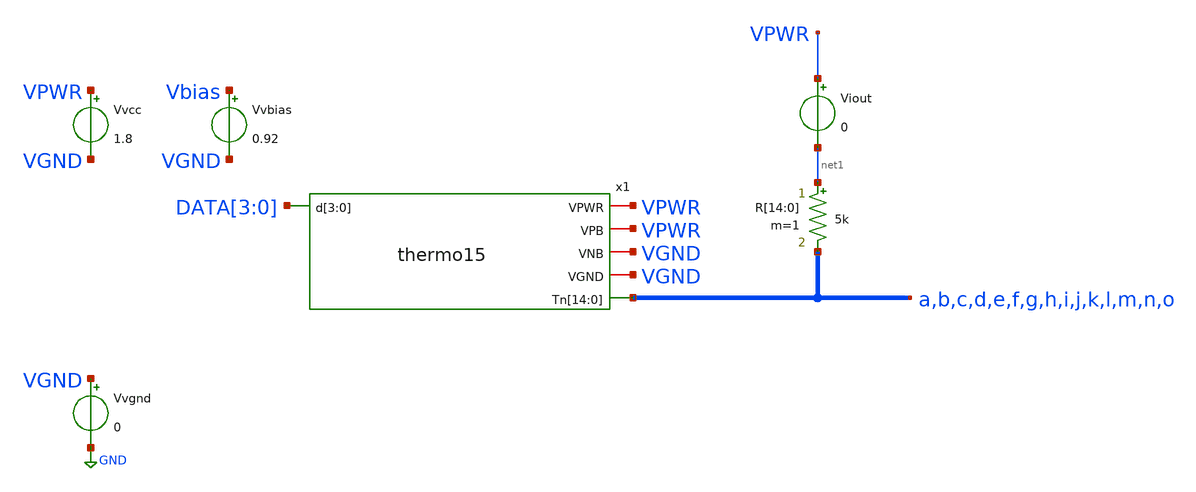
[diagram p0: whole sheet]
** sch_path: xschem/tb_thermo15.sch
**.subckt tb_thermo15
Vvcc VPWR VGND 1.8
R[14] net1 a 5k m=1
R[13] net1 b 5k m=1
R[12] net1 c 5k m=1
R[11] net1 d 5k m=1
R[10] net1 e 5k m=1
R[9] net1 f 5k m=1
R[8] net1 g 5k m=1
R[7] net1 h 5k m=1
R[6] net1 i 5k m=1
R[5] net1 j 5k m=1
R[4] net1 k 5k m=1
R[3] net1 l 5k m=1
R[2] net1 m 5k m=1
R[1] net1 n 5k m=1
R[0] net1 o 5k m=1
Vvbias Vbias VGND 0.92
Vvgnd VGND GND 0
Viout VPWR net1 0
x1 VPWR VGND VPWR VGND a b c d e f g h i j k l m n o DATA[3] DATA[2] DATA[1] DATA[0] thermo15
**** begin user architecture code



Vxp0 DATA[0]  GND pulse 1.8v 0v 0n 1n 1n 39n 80n
Vxp1 DATA[1]  GND pulse 1.8v 0v 0n 1n 1n 79n 160n
Vxp2 DATA[2]  GND pulse 1.8v 0v 0n 1n 1n 159n 320n
Vxp3 DATA[3]  GND pulse 1.8v 0v 0n 1n 1n 319n 640n

*.options savecurrents
.control

    save all
    tran 1n 12.8u
    write tb_row15x.raw a b c d e f g h i j k l m n o

.endc




.lib $::SKYWATER_MODELS/sky130.lib.spice tt
.include $::SKYWATER_STDCELLS/sky130_fd_sc_hd.spice

**** end user architecture code
**.ends

* expanding   symbol:  thermo15.sym # of pins=6
** sym_path: xschem/thermo15.sym
** sch_path: xschem/thermo15.sch
.subckt thermo15 VPWR VGND VPB VNB Tn[14] Tn[13] Tn[12] Tn[11] Tn[10] Tn[9] Tn[8] Tn[7] Tn[6] Tn[5]
+ Tn[4] Tn[3] Tn[2] Tn[1] Tn[0] d[3] d[2] d[1] d[0]
*.iopin VPWR
*.ipin d[3],d[2],d[1],d[0]
*.iopin VGND
*.iopin VPB
*.iopin VNB
*.opin
*+ Tn[14],Tn[13],Tn[12],Tn[11],Tn[10],Tn[9],Tn[8],Tn[7],Tn[6],Tn[5],Tn[4],Tn[3],Tn[2],Tn[1],Tn[0]
x1 d[1] VGND VNB VPB VPWR net3 sky130_fd_sc_hd__inv_1
x2 net5 VGND VNB VPB VPWR net6 sky130_fd_sc_hd__inv_2
x3 d[0] d[1] VGND VNB VPB VPWR net4 sky130_fd_sc_hd__nand2_1
x4 d[0] d[1] VGND VNB VPB VPWR net2 sky130_fd_sc_hd__nor2_1
x5 d[2] VGND VNB VPB VPWR net1 sky130_fd_sc_hd__inv_1
x6 net2 net1 VGND VNB VPB VPWR net7 sky130_fd_sc_hd__nand2_1
x7 net3 net1 VGND VNB VPB VPWR net8 sky130_fd_sc_hd__nand2_1
x8 net4 net1 VGND VNB VPB VPWR net9 sky130_fd_sc_hd__nand2_1
x9 net1 VGND VNB VPB VPWR net10 sky130_fd_sc_hd__inv_1
x10 net2 net1 VGND VNB VPB VPWR net11 sky130_fd_sc_hd__nor2_1
x11 net3 net1 VGND VNB VPB VPWR net12 sky130_fd_sc_hd__nor2_1
x12 net4 net1 VGND VNB VPB VPWR net13 sky130_fd_sc_hd__nor2_1
x13 net7 net6 VGND VNB VPB VPWR Tn[0] sky130_fd_sc_hd__nor2_4
x14 net8 net6 VGND VNB VPB VPWR Tn[1] sky130_fd_sc_hd__nor2_4
x15 net9 net6 VGND VNB VPB VPWR Tn[2] sky130_fd_sc_hd__nor2_4
x16 net10 net6 VGND VNB VPB VPWR Tn[3] sky130_fd_sc_hd__nor2_4
x17 net11 net6 VGND VNB VPB VPWR Tn[4] sky130_fd_sc_hd__nor2_4
x18 net12 net6 VGND VNB VPB VPWR Tn[5] sky130_fd_sc_hd__nor2_4
x19 net13 net6 VGND VNB VPB VPWR Tn[6] sky130_fd_sc_hd__nor2_4
x20 net6 VGND VNB VPB VPWR Tn[7] sky130_fd_sc_hd__inv_4
x21 net7 net6 VGND VNB VPB VPWR Tn[8] sky130_fd_sc_hd__nand2_4
x22 net8 net6 VGND VNB VPB VPWR Tn[9] sky130_fd_sc_hd__nand2_4
x23 net9 net6 VGND VNB VPB VPWR Tn[10] sky130_fd_sc_hd__nand2_4
x24 net10 net6 VGND VNB VPB VPWR Tn[11] sky130_fd_sc_hd__nand2_4
x25 net11 net6 VGND VNB VPB VPWR Tn[12] sky130_fd_sc_hd__nand2_4
x26 net12 net6 VGND VNB VPB VPWR Tn[13] sky130_fd_sc_hd__nand2_4
x27 net13 net6 VGND VNB VPB VPWR Tn[14] sky130_fd_sc_hd__nand2_4
x28 d[3] VGND VNB VPB VPWR net5 sky130_fd_sc_hd__inv_1
.ends

.GLOBAL GND
.end
